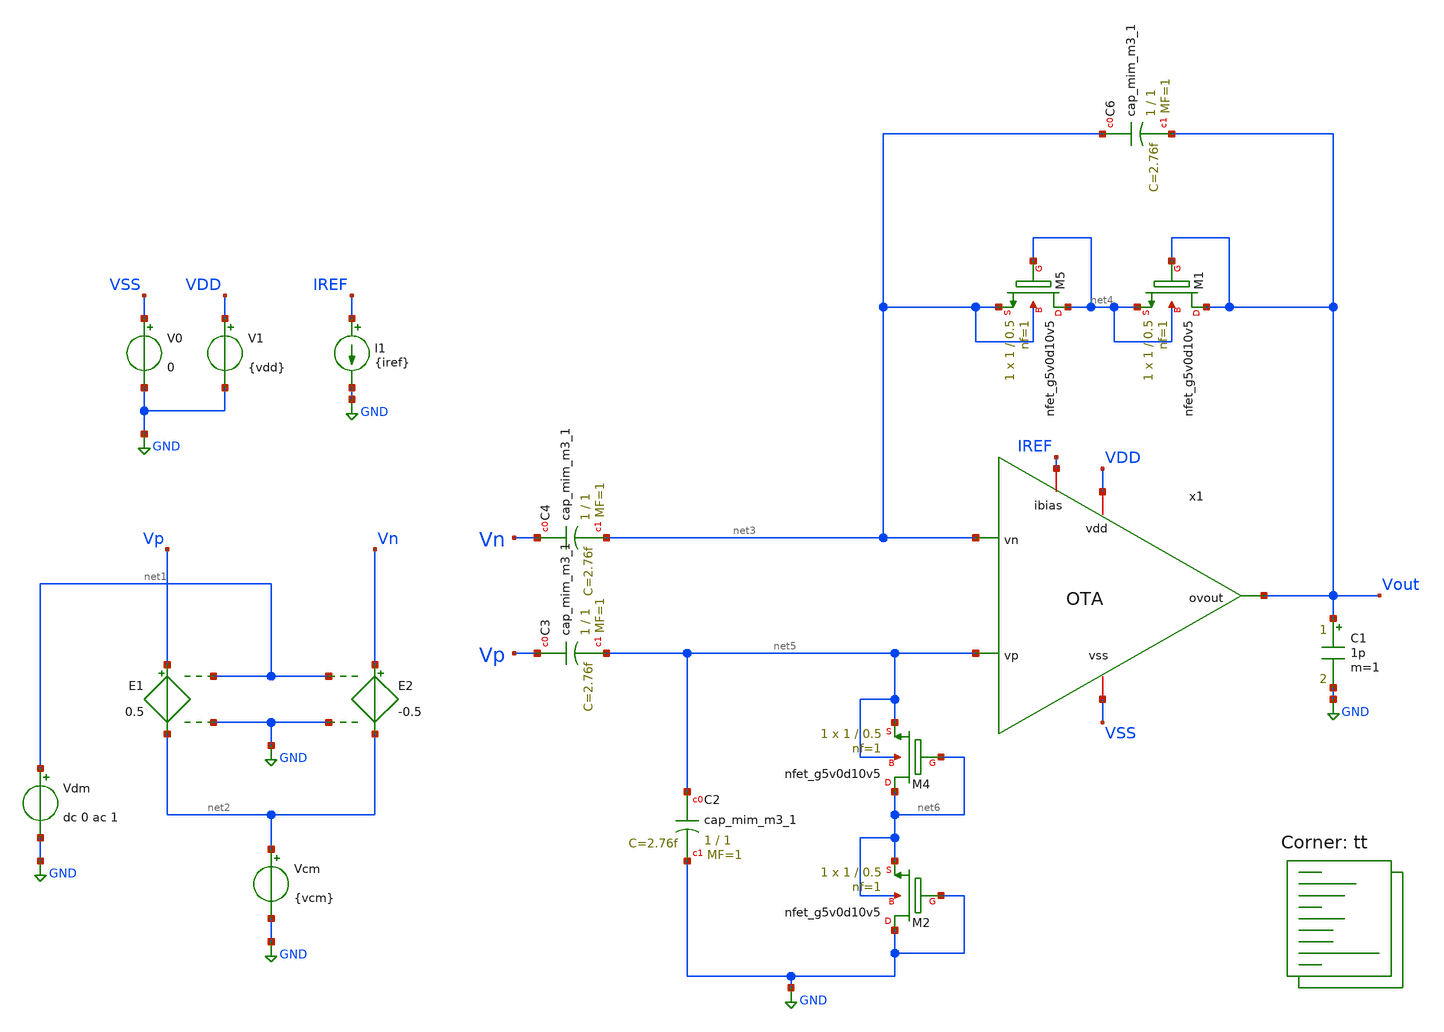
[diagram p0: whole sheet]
** sch_path: xschem/LNA_tb.sch
**.subckt LNA_tb
V0 VSS GND 0
V1 VDD GND {vdd}
E1 Vp net2 net1 GND 0.5
E2 Vn net2 net1 GND -0.5
Vdm net1 GND dc 0 ac 1
Vcm net2 GND {vcm}
C1 Vout GND 1p m=1
XC6 net3 Vout sky130_fd_pr__cap_mim_m3_1 W=1 L=1 MF=1 m=1
XC2 net5 GND sky130_fd_pr__cap_mim_m3_1 W=1 L=1 MF=1 m=1
XC3 Vp net5 sky130_fd_pr__cap_mim_m3_1 W=1 L=1 MF=1 m=1
XC4 Vn net3 sky130_fd_pr__cap_mim_m3_1 W=1 L=1 MF=1 m=1
XM5 net4 net4 net3 net3 sky130_fd_pr__nfet_g5v0d10v5 L=0.5 W=1 nf=1 ad='int((nf+1)/2) * W/nf * 0.29'
+ as='int((nf+2)/2) * W/nf * 0.29' pd='2*int((nf+1)/2) * (W/nf + 0.29)' ps='2*int((nf+2)/2) * (W/nf + 0.29)'
+ nrd='0.29 / W' nrs='0.29 / W' sa=0 sb=0 sd=0 mult=1 m=1
XM1 Vout Vout net4 net4 sky130_fd_pr__nfet_g5v0d10v5 L=0.5 W=1 nf=1 ad='int((nf+1)/2) * W/nf * 0.29'
+ as='int((nf+2)/2) * W/nf * 0.29' pd='2*int((nf+1)/2) * (W/nf + 0.29)' ps='2*int((nf+2)/2) * (W/nf + 0.29)'
+ nrd='0.29 / W' nrs='0.29 / W' sa=0 sb=0 sd=0 mult=1 m=1
XM4 net6 net6 net5 net5 sky130_fd_pr__nfet_g5v0d10v5 L=0.5 W=1 nf=1 ad='int((nf+1)/2) * W/nf * 0.29'
+ as='int((nf+2)/2) * W/nf * 0.29' pd='2*int((nf+1)/2) * (W/nf + 0.29)' ps='2*int((nf+2)/2) * (W/nf + 0.29)'
+ nrd='0.29 / W' nrs='0.29 / W' sa=0 sb=0 sd=0 mult=1 m=1
XM2 GND GND net6 net6 sky130_fd_pr__nfet_g5v0d10v5 L=0.5 W=1 nf=1 ad='int((nf+1)/2) * W/nf * 0.29' as='int((nf+2)/2) * W/nf * 0.29'
+ pd='2*int((nf+1)/2) * (W/nf + 0.29)' ps='2*int((nf+2)/2) * (W/nf + 0.29)' nrd='0.29 / W' nrs='0.29 / W'
+ sa=0 sb=0 sd=0 mult=1 m=1
I1 IREF GND {iref}
x1 Vout VDD VSS IREF net3 net5 OTA
**** begin user architecture code

.param vdd=5
.param vcm=2.5
.param iref = 1u

.control
	save all
	save @m.x1.xm1a.msky130_fd_pr__pfet_g5v0d10v5[id] @m.x1.xm1a.msky130_fd_pr__pfet_g5v0d10v5[gm]
+ @m.x1.xm1a.msky130_fd_pr__pfet_g5v0d10v5[gds]
	save @m.x1.xm1b.msky130_fd_pr__pfet_g5v0d10v5[id] @m.x1.xm1b.msky130_fd_pr__pfet_g5v0d10v5[gm]
+ @m.x1.xm1b.msky130_fd_pr__pfet_g5v0d10v5[gds]
	save @m.x1.xm2a.msky130_fd_pr__pfet_g5v0d10v5[id] @m.x1.xm2a.msky130_fd_pr__pfet_g5v0d10v5[gm]
+ @m.x1.xm2a.msky130_fd_pr__pfet_g5v0d10v5[gds]
	save @m.x1.xm2b.msky130_fd_pr__pfet_g5v0d10v5[id] @m.x1.xm2b.msky130_fd_pr__pfet_g5v0d10v5[gm]
+ @m.x1.xm2b.msky130_fd_pr__pfet_g5v0d10v5[gds]
	save @m.x1.xm3a.msky130_fd_pr__nfet_g5v0d10v5[id] @m.x1.xm3a.msky130_fd_pr__nfet_g5v0d10v5[gm]
+ @m.x1.xm3a.msky130_fd_pr__nfet_g5v0d10v5[gds]
	save @m.x1.xm3b.msky130_fd_pr__nfet_g5v0d10v5[id] @m.x1.xm3b.msky130_fd_pr__nfet_g5v0d10v5[gm]
+ @m.x1.xm3b.msky130_fd_pr__nfet_g5v0d10v5[gds]
	save @m.x1.xm4a.msky130_fd_pr__nfet_g5v0d10v5[id] @m.x1.xm4a.msky130_fd_pr__nfet_g5v0d10v5[gm]
+ @m.x1.xm4a.msky130_fd_pr__nfet_g5v0d10v5[gds]
	save @m.x1.xm4b.msky130_fd_pr__nfet_g5v0d10v5[id] @m.x1.xm4b.msky130_fd_pr__nfet_g5v0d10v5[gm]
+ @m.x1.xm4b.msky130_fd_pr__nfet_g5v0d10v5[gds]
	save @m.x1.xm4c.msky130_fd_pr__nfet_g5v0d10v5[id] @m.x1.xm4c.msky130_fd_pr__nfet_g5v0d10v5[gm]
+ @m.x1.xm4c.msky130_fd_pr__nfet_g5v0d10v5[gds]
	save @m.x1.xm4d.msky130_fd_pr__nfet_g5v0d10v5[id] @m.x1.xm4d.msky130_fd_pr__nfet_g5v0d10v5[gm]
+ @m.x1.xm4d.msky130_fd_pr__nfet_g5v0d10v5[gds]
	save @m.x1.xm5a.msky130_fd_pr__pfet_g5v0d10v5[id] @m.x1.xm5a.msky130_fd_pr__pfet_g5v0d10v5[gm]
+ @m.x1.xm5a.msky130_fd_pr__pfet_g5v0d10v5[gds]
	save @m.x1.xm5b.msky130_fd_pr__pfet_g5v0d10v5[id] @m.x1.xm5b.msky130_fd_pr__pfet_g5v0d10v5[gm]
+ @m.x1.xm5b.msky130_fd_pr__pfet_g5v0d10v5[gds]
	save @m.x1.xm6.msky130_fd_pr__pfet_g5v0d10v5[id] @m.x1.xm6.msky130_fd_pr__pfet_g5v0d10v5[gm]
+ @m.x1.xm6.msky130_fd_pr__pfet_g5v0d10v5[gds]
	save @m.x1.xm7.msky130_fd_pr__pfet_g5v0d10v5[id] @m.x1.xm7.msky130_fd_pr__pfet_g5v0d10v5[gm]
+ @m.x1.xm7.msky130_fd_pr__pfet_g5v0d10v5[gds]

	op
	show

	ac oct 10 0.1 10e3
	let vout_mag = abs(v(Vout))
	*plot vout_mag
	let vout_phase_margin = phase(v(Vout)) * 180/pi + 180
	*plot vout_phase_margin
	meas ac A0 find vout_mag at=1k
	meas ac UGF when vout_mag=1 fall=1
	meas ac PM find vout_phase_margin when vout_mag=1

	echo $plots
	write LNA_tb.raw

.endc



.lib $::SKYWATER_MODELS/sky130.lib.spice tt
**** end user architecture code
**.ends

* expanding   symbol:  /home/william/projects/sky130_vbl_ip__LNA/xschem/OTA.sym # of pins=6
** sym_path: xschem/OTA.sym
** sch_path: xschem/OTA.sch
.subckt OTA ovout vdd vss ibias vn vp
*.iopin ibias
*.iopin vdd
*.iopin vss
*.ipin vp
*.ipin vn
*.opin ovout
XM5a net2 vp net1 vdd sky130_fd_pr__pfet_g5v0d10v5 L=0.5 W=80 nf=1 ad='int((nf+1)/2) * W/nf * 0.29' as='int((nf+2)/2) * W/nf * 0.29'
+ pd='2*int((nf+1)/2) * (W/nf + 0.29)' ps='2*int((nf+2)/2) * (W/nf + 0.29)' nrd='0.29 / W' nrs='0.29 / W'
+ sa=0 sb=0 sd=0 mult=1 m=1
XM5b net3 vn net1 vdd sky130_fd_pr__pfet_g5v0d10v5 L=0.5 W=80 nf=1 ad='int((nf+1)/2) * W/nf * 0.29' as='int((nf+2)/2) * W/nf * 0.29'
+ pd='2*int((nf+1)/2) * (W/nf + 0.29)' ps='2*int((nf+2)/2) * (W/nf + 0.29)' nrd='0.29 / W' nrs='0.29 / W'
+ sa=0 sb=0 sd=0 mult=1 m=1
XM4b net2 net2 vss vss sky130_fd_pr__nfet_g5v0d10v5 L=4 W=1 nf=1 ad='int((nf+1)/2) * W/nf * 0.29' as='int((nf+2)/2) * W/nf * 0.29'
+ pd='2*int((nf+1)/2) * (W/nf + 0.29)' ps='2*int((nf+2)/2) * (W/nf + 0.29)' nrd='0.29 / W' nrs='0.29 / W'
+ sa=0 sb=0 sd=0 mult=1 m=1
XM4c net3 net3 vss vss sky130_fd_pr__nfet_g5v0d10v5 L=4 W=1 nf=1 ad='int((nf+1)/2) * W/nf * 0.29' as='int((nf+2)/2) * W/nf * 0.29'
+ pd='2*int((nf+1)/2) * (W/nf + 0.29)' ps='2*int((nf+2)/2) * (W/nf + 0.29)' nrd='0.29 / W' nrs='0.29 / W'
+ sa=0 sb=0 sd=0 mult=1 m=1
XM4a net5 net2 vss vss sky130_fd_pr__nfet_g5v0d10v5 L=4 W=1 nf=1 ad='int((nf+1)/2) * W/nf * 0.29' as='int((nf+2)/2) * W/nf * 0.29'
+ pd='2*int((nf+1)/2) * (W/nf + 0.29)' ps='2*int((nf+2)/2) * (W/nf + 0.29)' nrd='0.29 / W' nrs='0.29 / W'
+ sa=0 sb=0 sd=0 mult=1 m=1
XM4d net7 net3 vss vss sky130_fd_pr__nfet_g5v0d10v5 L=4 W=1 nf=1 ad='int((nf+1)/2) * W/nf * 0.29' as='int((nf+2)/2) * W/nf * 0.29'
+ pd='2*int((nf+1)/2) * (W/nf + 0.29)' ps='2*int((nf+2)/2) * (W/nf + 0.29)' nrd='0.29 / W' nrs='0.29 / W'
+ sa=0 sb=0 sd=0 mult=1 m=1
XM1a net4 net4 vdd vdd sky130_fd_pr__pfet_g5v0d10v5 L=1 W=0.6 nf=1 ad='int((nf+1)/2) * W/nf * 0.29' as='int((nf+2)/2) * W/nf * 0.29'
+ pd='2*int((nf+1)/2) * (W/nf + 0.29)' ps='2*int((nf+2)/2) * (W/nf + 0.29)' nrd='0.29 / W' nrs='0.29 / W'
+ sa=0 sb=0 sd=0 mult=1 m=1
XM1b net8 net4 vdd vdd sky130_fd_pr__pfet_g5v0d10v5 L=1 W=0.6 nf=1 ad='int((nf+1)/2) * W/nf * 0.29' as='int((nf+2)/2) * W/nf * 0.29'
+ pd='2*int((nf+1)/2) * (W/nf + 0.29)' ps='2*int((nf+2)/2) * (W/nf + 0.29)' nrd='0.29 / W' nrs='0.29 / W'
+ sa=0 sb=0 sd=0 mult=1 m=1
XM7 ibias ibias vdd vdd sky130_fd_pr__pfet_g5v0d10v5 L=2 W=2 nf=1 ad='int((nf+1)/2) * W/nf * 0.29' as='int((nf+2)/2) * W/nf * 0.29'
+ pd='2*int((nf+1)/2) * (W/nf + 0.29)' ps='2*int((nf+2)/2) * (W/nf + 0.29)' nrd='0.29 / W' nrs='0.29 / W'
+ sa=0 sb=0 sd=0 mult=1 m=1
XM6 net1 ibias vdd vdd sky130_fd_pr__pfet_g5v0d10v5 L=2 W=2 nf=1 ad='int((nf+1)/2) * W/nf * 0.29' as='int((nf+2)/2) * W/nf * 0.29'
+ pd='2*int((nf+1)/2) * (W/nf + 0.29)' ps='2*int((nf+2)/2) * (W/nf + 0.29)' nrd='0.29 / W' nrs='0.29 / W'
+ sa=0 sb=0 sd=0 mult=1 m=1
XM3a net6 net6 net5 vss sky130_fd_pr__nfet_g5v0d10v5 L=4 W=1 nf=1 ad='int((nf+1)/2) * W/nf * 0.29' as='int((nf+2)/2) * W/nf * 0.29'
+ pd='2*int((nf+1)/2) * (W/nf + 0.29)' ps='2*int((nf+2)/2) * (W/nf + 0.29)' nrd='0.29 / W' nrs='0.29 / W'
+ sa=0 sb=0 sd=0 mult=1 m=1
XM2a net6 net6 net4 vdd sky130_fd_pr__pfet_g5v0d10v5 L=1 W=0.6 nf=1 ad='int((nf+1)/2) * W/nf * 0.29'
+ as='int((nf+2)/2) * W/nf * 0.29' pd='2*int((nf+1)/2) * (W/nf + 0.29)' ps='2*int((nf+2)/2) * (W/nf + 0.29)'
+ nrd='0.29 / W' nrs='0.29 / W' sa=0 sb=0 sd=0 mult=1 m=1
XM2b ovout ovout net8 vdd sky130_fd_pr__pfet_g5v0d10v5 L=1 W=0.6 nf=1 ad='int((nf+1)/2) * W/nf * 0.29'
+ as='int((nf+2)/2) * W/nf * 0.29' pd='2*int((nf+1)/2) * (W/nf + 0.29)' ps='2*int((nf+2)/2) * (W/nf + 0.29)'
+ nrd='0.29 / W' nrs='0.29 / W' sa=0 sb=0 sd=0 mult=1 m=1
XM3b ovout ovout net7 vss sky130_fd_pr__nfet_g5v0d10v5 L=4 W=1 nf=1 ad='int((nf+1)/2) * W/nf * 0.29'
+ as='int((nf+2)/2) * W/nf * 0.29' pd='2*int((nf+1)/2) * (W/nf + 0.29)' ps='2*int((nf+2)/2) * (W/nf + 0.29)'
+ nrd='0.29 / W' nrs='0.29 / W' sa=0 sb=0 sd=0 mult=1 m=1
.ends

.GLOBAL GND
.end
